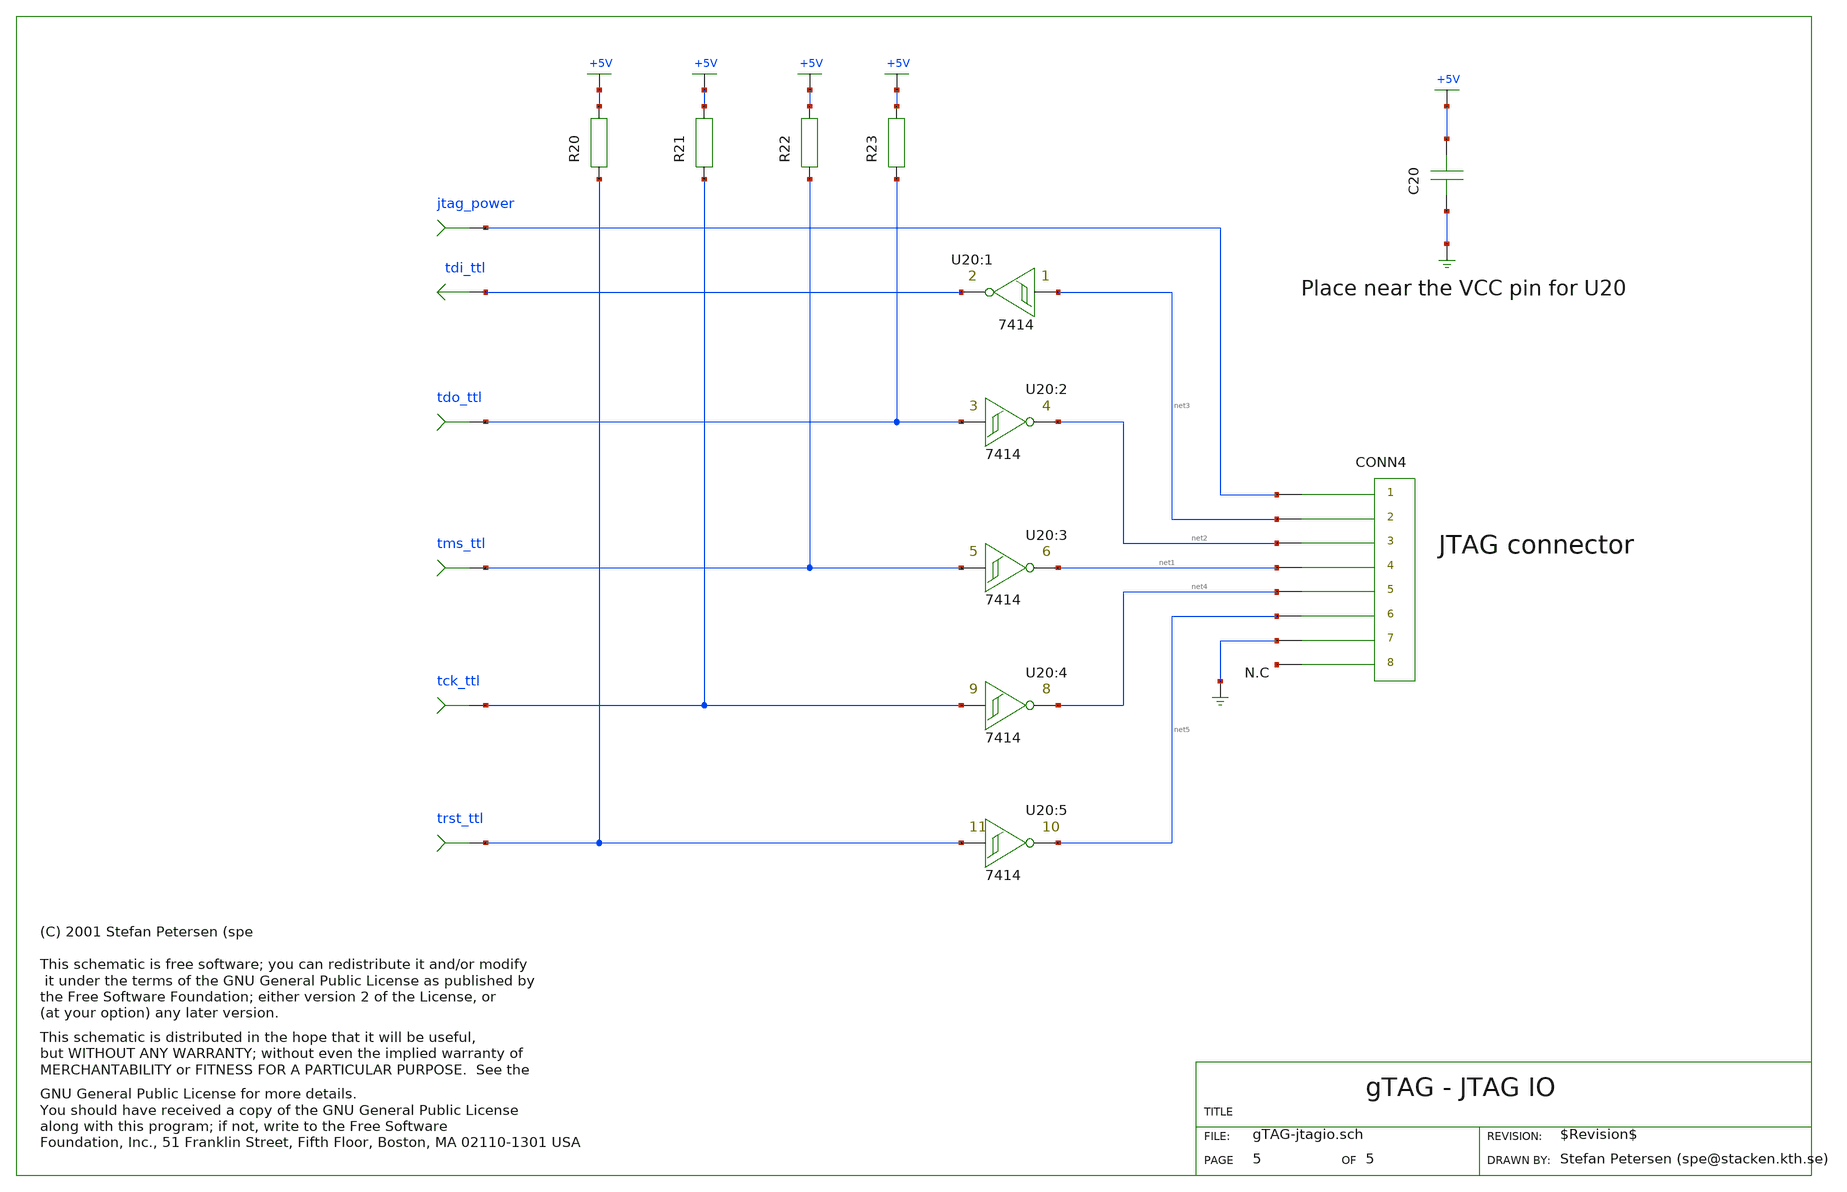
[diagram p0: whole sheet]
** sch_path: xschem-src/xschem_library/gschem_import/gTAG-jtagio.sch
* Copyright (C) 1998-2026 Stefan Frederik Schippers
* This program is free software; you can redistribute it and/or modify
* it under the terms of the GNU General Public License as published by
* the Free Software Foundation; either version 2 of the License, or
* (at your option) any later version.
* This program is distributed in the hope that it will be useful,
* but WITHOUT ANY WARRANTY; without even the implied warranty of
* MERCHANTABILITY or FITNESS FOR A PARTICULAR PURPOSE.  See the
* GNU General Public License for more details.
* You should have received a copy of the GNU General Public License
* along with this program; if not, write to the Free Software
* copyleft.sym
**.subckt gTAG-jtagio tdo_ttl tms_ttl tck_ttl trst_ttl jtag_power tdi_ttl
U20:1 net3 tdi_ttl
U20:2 tdo_ttl net2
U20:3 tms_ttl net1
U20:4 tck_ttl net4
U20:5 trst_ttl net5
CONN4 jtag_power net3 net2 net1 net4 net5 GND net6
CONN4
C20 GND +5V 100n
R20 trst_ttl +5V 10k
R21 tck_ttl +5V 10k
R22 tms_ttl +5V 10k
R23 tdo_ttl +5V 10k
**.ends
.end
